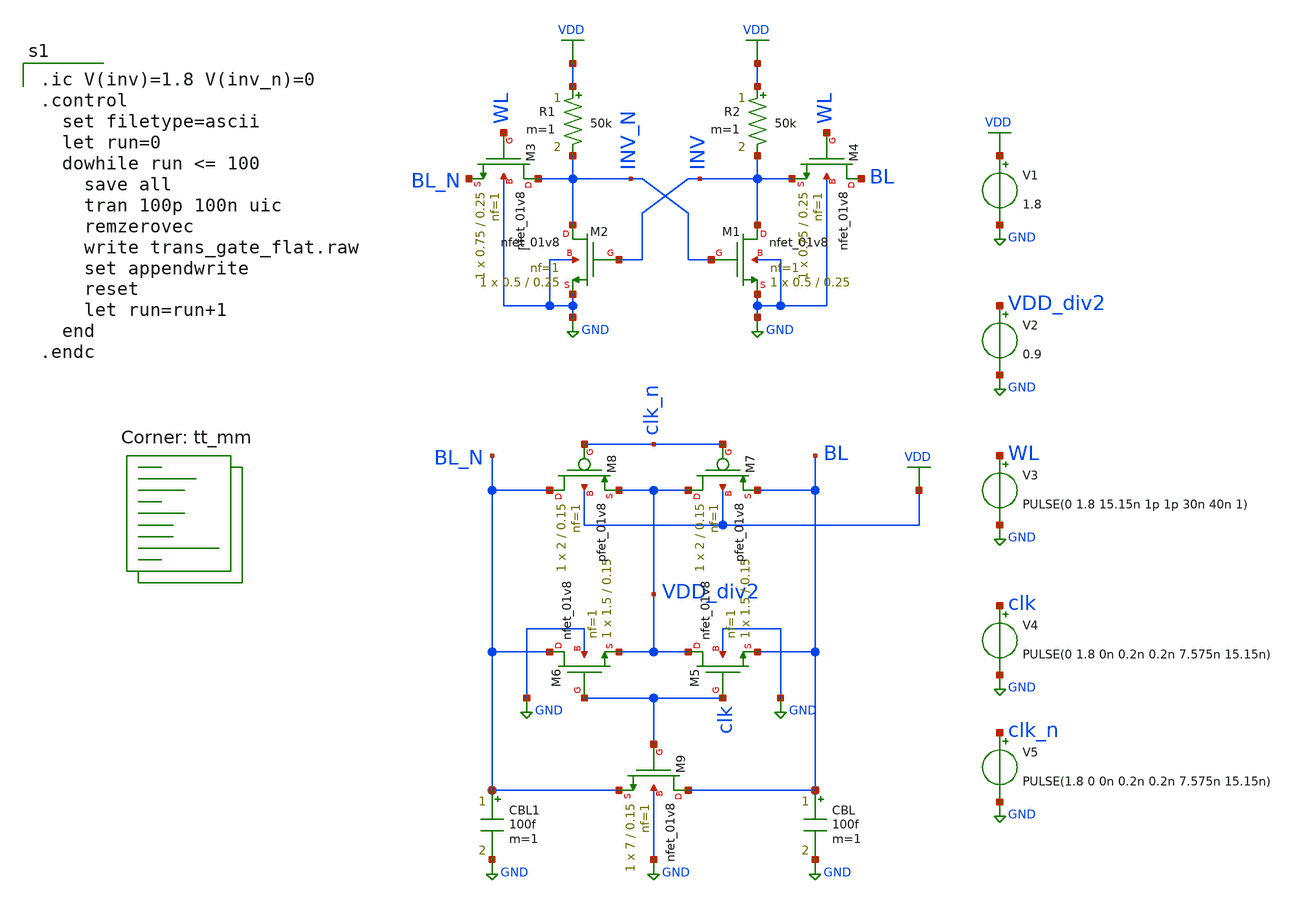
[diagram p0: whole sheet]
** sch_path: analog/schematics/trans_gate_flat.sch
**.subckt trans_gate_flat
R1 VDD INV_N 50k m=1
R2 VDD INV 50k m=1
V1 VDD GND 1.8
CBL BL GND 100f m=1
CBL1 BL_N GND 100f m=1
V2 VDD_div2 GND 0.9
V3 WL GND PULSE(0 1.8 15.15n 1p 1p 30n 40n 1)
V4 clk GND PULSE(0 1.8 0n 0.2n 0.2n 7.575n 15.15n)
V5 clk_n GND PULSE(1.8 0 0n 0.2n 0.2n 7.575n 15.15n)
XM1 INV INV_N GND GND sky130_fd_pr__nfet_01v8 L=0.25 W=0.5 nf=1 ad='int((nf+1)/2) * W/nf * 0.29' as='int((nf+2)/2) * W/nf * 0.29'
+ pd='2*int((nf+1)/2) * (W/nf + 0.29)' ps='2*int((nf+2)/2) * (W/nf + 0.29)' nrd='0.29 / W' nrs='0.29 / W'
+ sa=0 sb=0 sd=0 mult=1 m=1
XM3 INV_N WL BL_N GND sky130_fd_pr__nfet_01v8 L=0.25 W=0.75 nf=1 ad='int((nf+1)/2) * W/nf * 0.29' as='int((nf+2)/2) * W/nf * 0.29'
+ pd='2*int((nf+1)/2) * (W/nf + 0.29)' ps='2*int((nf+2)/2) * (W/nf + 0.29)' nrd='0.29 / W' nrs='0.29 / W'
+ sa=0 sb=0 sd=0 mult=1 m=1
XM4 BL WL INV GND sky130_fd_pr__nfet_01v8 L=0.25 W=0.75 nf=1 ad='int((nf+1)/2) * W/nf * 0.29' as='int((nf+2)/2) * W/nf * 0.29'
+ pd='2*int((nf+1)/2) * (W/nf + 0.29)' ps='2*int((nf+2)/2) * (W/nf + 0.29)' nrd='0.29 / W' nrs='0.29 / W'
+ sa=0 sb=0 sd=0 mult=1 m=1
XM5 VDD_div2 clk BL GND sky130_fd_pr__nfet_01v8 L=0.15 W=1.5 nf=1 ad='int((nf+1)/2) * W/nf * 0.29' as='int((nf+2)/2) * W/nf * 0.29'
+ pd='2*int((nf+1)/2) * (W/nf + 0.29)' ps='2*int((nf+2)/2) * (W/nf + 0.29)' nrd='0.29 / W' nrs='0.29 / W'
+ sa=0 sb=0 sd=0 mult=1 m=1
XM6 BL_N clk VDD_div2 GND sky130_fd_pr__nfet_01v8 L=0.15 W=1.5 nf=1 ad='int((nf+1)/2) * W/nf * 0.29'
+ as='int((nf+2)/2) * W/nf * 0.29' pd='2*int((nf+1)/2) * (W/nf + 0.29)' ps='2*int((nf+2)/2) * (W/nf + 0.29)'
+ nrd='0.29 / W' nrs='0.29 / W' sa=0 sb=0 sd=0 mult=1 m=1
XM7 VDD_div2 clk_n BL VDD sky130_fd_pr__pfet_01v8 L=0.15 W=2 nf=1 ad='int((nf+1)/2) * W/nf * 0.29' as='int((nf+2)/2) * W/nf * 0.29'
+ pd='2*int((nf+1)/2) * (W/nf + 0.29)' ps='2*int((nf+2)/2) * (W/nf + 0.29)' nrd='0.29 / W' nrs='0.29 / W'
+ sa=0 sb=0 sd=0 mult=1 m=1
XM8 BL_N clk_n VDD_div2 VDD sky130_fd_pr__pfet_01v8 L=0.15 W=2 nf=1 ad='int((nf+1)/2) * W/nf * 0.29'
+ as='int((nf+2)/2) * W/nf * 0.29' pd='2*int((nf+1)/2) * (W/nf + 0.29)' ps='2*int((nf+2)/2) * (W/nf + 0.29)'
+ nrd='0.29 / W' nrs='0.29 / W' sa=0 sb=0 sd=0 mult=1 m=1
XM9 BL clk BL_N GND sky130_fd_pr__nfet_01v8 L=0.15 W=7 nf=1 ad='int((nf+1)/2) * W/nf * 0.29' as='int((nf+2)/2) * W/nf * 0.29'
+ pd='2*int((nf+1)/2) * (W/nf + 0.29)' ps='2*int((nf+2)/2) * (W/nf + 0.29)' nrd='0.29 / W' nrs='0.29 / W'
+ sa=0 sb=0 sd=0 mult=1 m=1
XM2 INV_N INV GND GND sky130_fd_pr__nfet_01v8 L=0.25 W=0.5 nf=1 ad='int((nf+1)/2) * W/nf * 0.29' as='int((nf+2)/2) * W/nf * 0.29'
+ pd='2*int((nf+1)/2) * (W/nf + 0.29)' ps='2*int((nf+2)/2) * (W/nf + 0.29)' nrd='0.29 / W' nrs='0.29 / W'
+ sa=0 sb=0 sd=0 mult=1 m=1
**** begin user architecture code

.ic V(inv)=1.8 V(inv_n)=0
.control
  set filetype=ascii
  let run=0
  dowhile run <= 100
    save all
    tran 100p 100n uic
    remzerovec
    write trans_gate_flat.raw
    set appendwrite
    reset
    let run=run+1
  end
.endc

.lib $::SKYWATER_MODELS/sky130.lib.spice tt_mm
**** end user architecture code
**.ends
.GLOBAL VDD
.GLOBAL GND
.end
